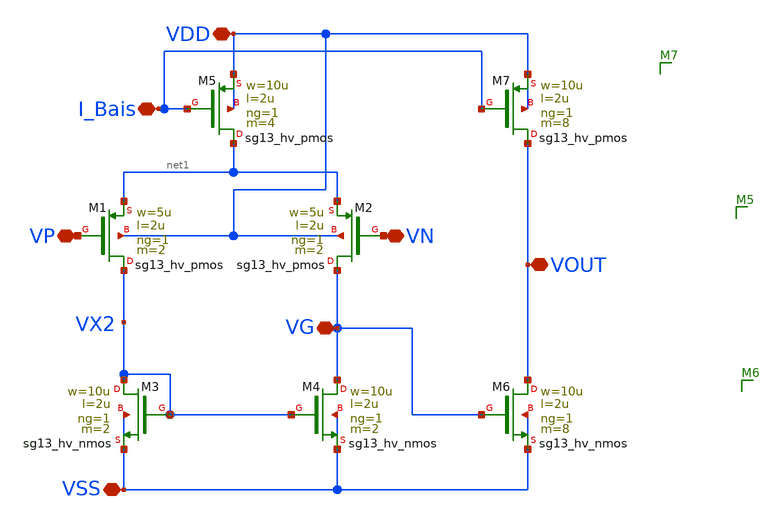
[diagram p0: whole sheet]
** sch_path: dependencies/PMU/PMU-main/schematic/xschem/OpAmp_2etags.sch
**.subckt OpAmp_2etags VDD I_Bais VP VN VG VOUT VSS
*.iopin VDD
*.iopin I_Bais
*.iopin VP
*.iopin VN
*.iopin VG
*.iopin VOUT
*.iopin VSS
XM3 VX2 VX2 VSS VSS sg13_hv_nmos w=10u l=2u ng=1 m=2 mm_ok=1
XM1 VX2 VP net1 VDD sg13_hv_pmos w=5u l=2u ng=1 m=2 mm_ok=1
XM2 VG VN net1 VDD sg13_hv_pmos w=5u l=2u ng=1 m=2 mm_ok=1
XM4 VG VX2 VSS VSS sg13_hv_nmos w=10u l=2u ng=1 m=2 mm_ok=1
XM5 net1 I_Bais VDD VDD sg13_hv_pmos w=10u l=2u ng=1 m=4 mm_ok=1
XM7 VOUT I_Bais VDD VDD sg13_hv_pmos w=10u l=2u ng=1 m=8 mm_ok=1
XM6 VOUT VG VSS VSS sg13_hv_nmos w=10u l=2u ng=1 m=8 mm_ok=1
**.ends
.end
